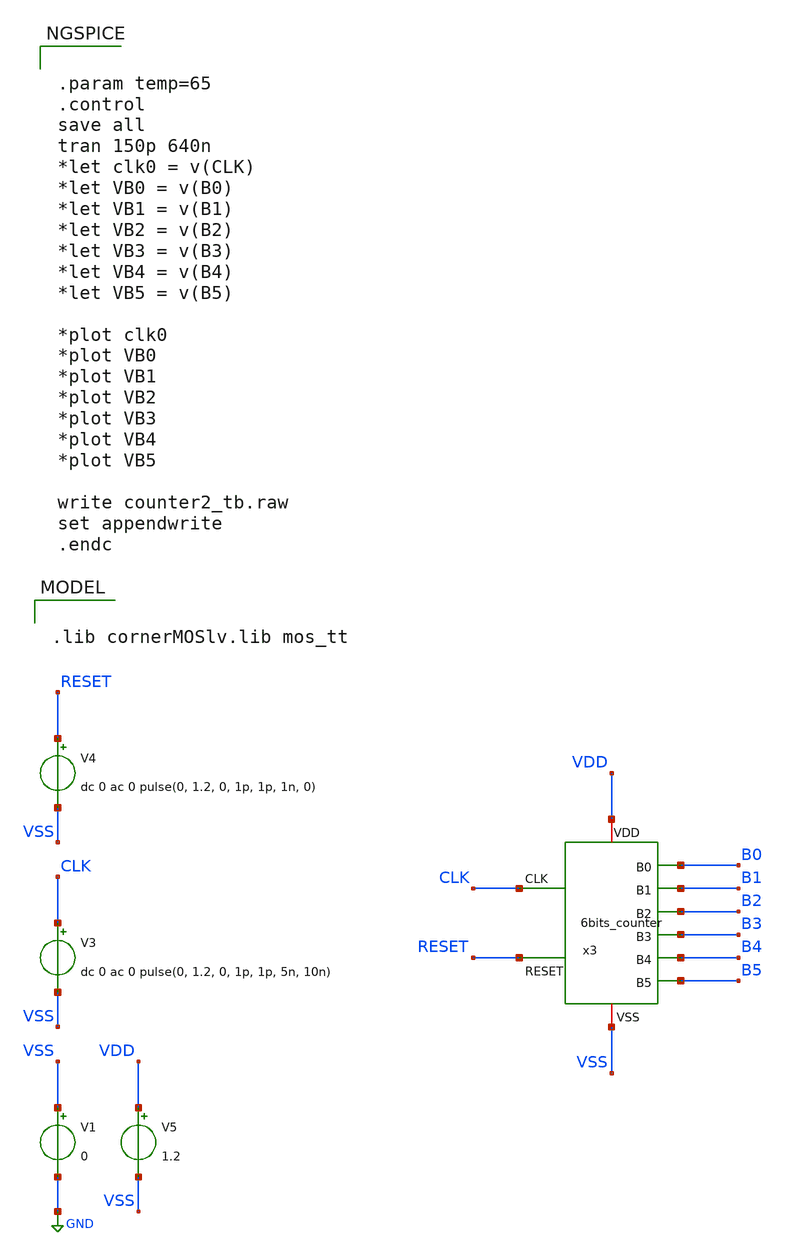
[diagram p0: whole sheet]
** sch_path: GROTDC/GROTDC_SIM/counter2_tb.sch
**.subckt counter2_tb
V1 VSS GND 0
V3 CLK VSS dc 0 ac 0 pulse(0, 1.2, 0, 1p, 1p, 5n, 10n)
V5 VDD VSS 1.2
V4 RESET VSS dc 0 ac 0 pulse(0, 1.2, 0, 1p, 1p, 1n, 0)
x3 B0 CLK VDD B1 B2 VSS RESET B3 B4 B5 6bits_counter
**** begin user architecture code


.param temp=65
.control
save all
tran 150p 640n
*let clk0 = v(CLK)
*let VB0 = v(B0)
*let VB1 = v(B1)
*let VB2 = v(B2)
*let VB3 = v(B3)
*let VB4 = v(B4)
*let VB5 = v(B5)

*plot clk0
*plot VB0
*plot VB1
*plot VB2
*plot VB3
*plot VB4
*plot VB5

write counter2_tb.raw
set appendwrite
.endc



.lib cornerMOSlv.lib mos_tt

**** end user architecture code
**.ends
.GLOBAL GND
.end
